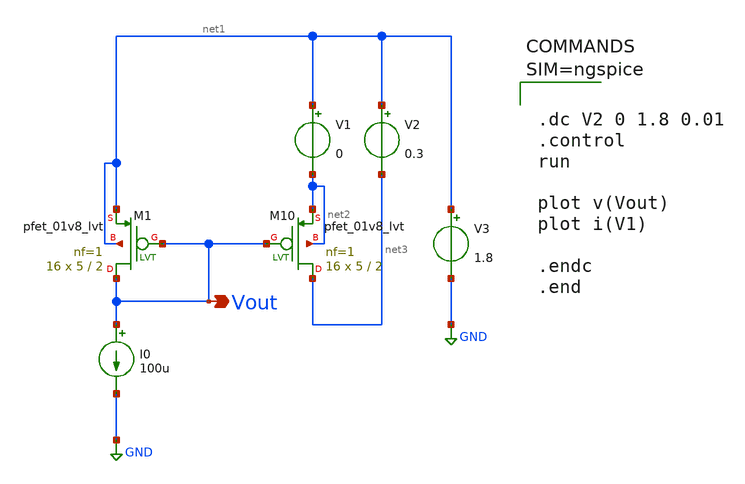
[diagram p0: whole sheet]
** sch_path: sch/Current-mirror_PMOS.sch
**.subckt Current-mirror_PMOS Vout
*.opin Vout
XM10 net3 Vout net2 net2 sky130_fd_pr__pfet_01v8_lvt L=2 W=5 nf=1 ad='int((1 + 1)/2) * 5 / 1 * 0.29'
+ as='int((1 + 2)/2) * 5 / 1 * 0.29' pd='2*int((1 + 1)/2) * (5 / 1 + 0.29)' ps='2*int((1 + 2)/2) * (5 / 1 + 0.29)'
+ nrd='0.29 / 5 ' nrs='0.29 / 5 ' sa=0 sb=0 sd=0 mult=16 m=16
XM1 Vout Vout net1 net1 sky130_fd_pr__pfet_01v8_lvt L=2 W=5 nf=1 ad='int((1 + 1)/2) * 5 / 1 * 0.29' as='int((1 + 2)/2) * 5 / 1 * 0.29'
+ pd='2*int((1 + 1)/2) * (5 / 1 + 0.29)' ps='2*int((1 + 2)/2) * (5 / 1 + 0.29)' nrd='0.29 / 5 ' nrs='0.29 / 5 '
+ sa=0 sb=0 sd=0 mult=16 m=16
I0 Vout GND 100u
V1 net1 net2 0
V2 net1 net3 0.3
V3 net1 GND 1.8
**** begin user architecture code

** opencircuitdesign pdks install
.lib $::SKYWATER_MODELS/sky130.lib.spice tt




.dc V2 0 1.8 0.01
.control
run

plot v(Vout)
plot i(V1)

.endc
.end



**** end user architecture code
**.ends
.GLOBAL GND
.end
